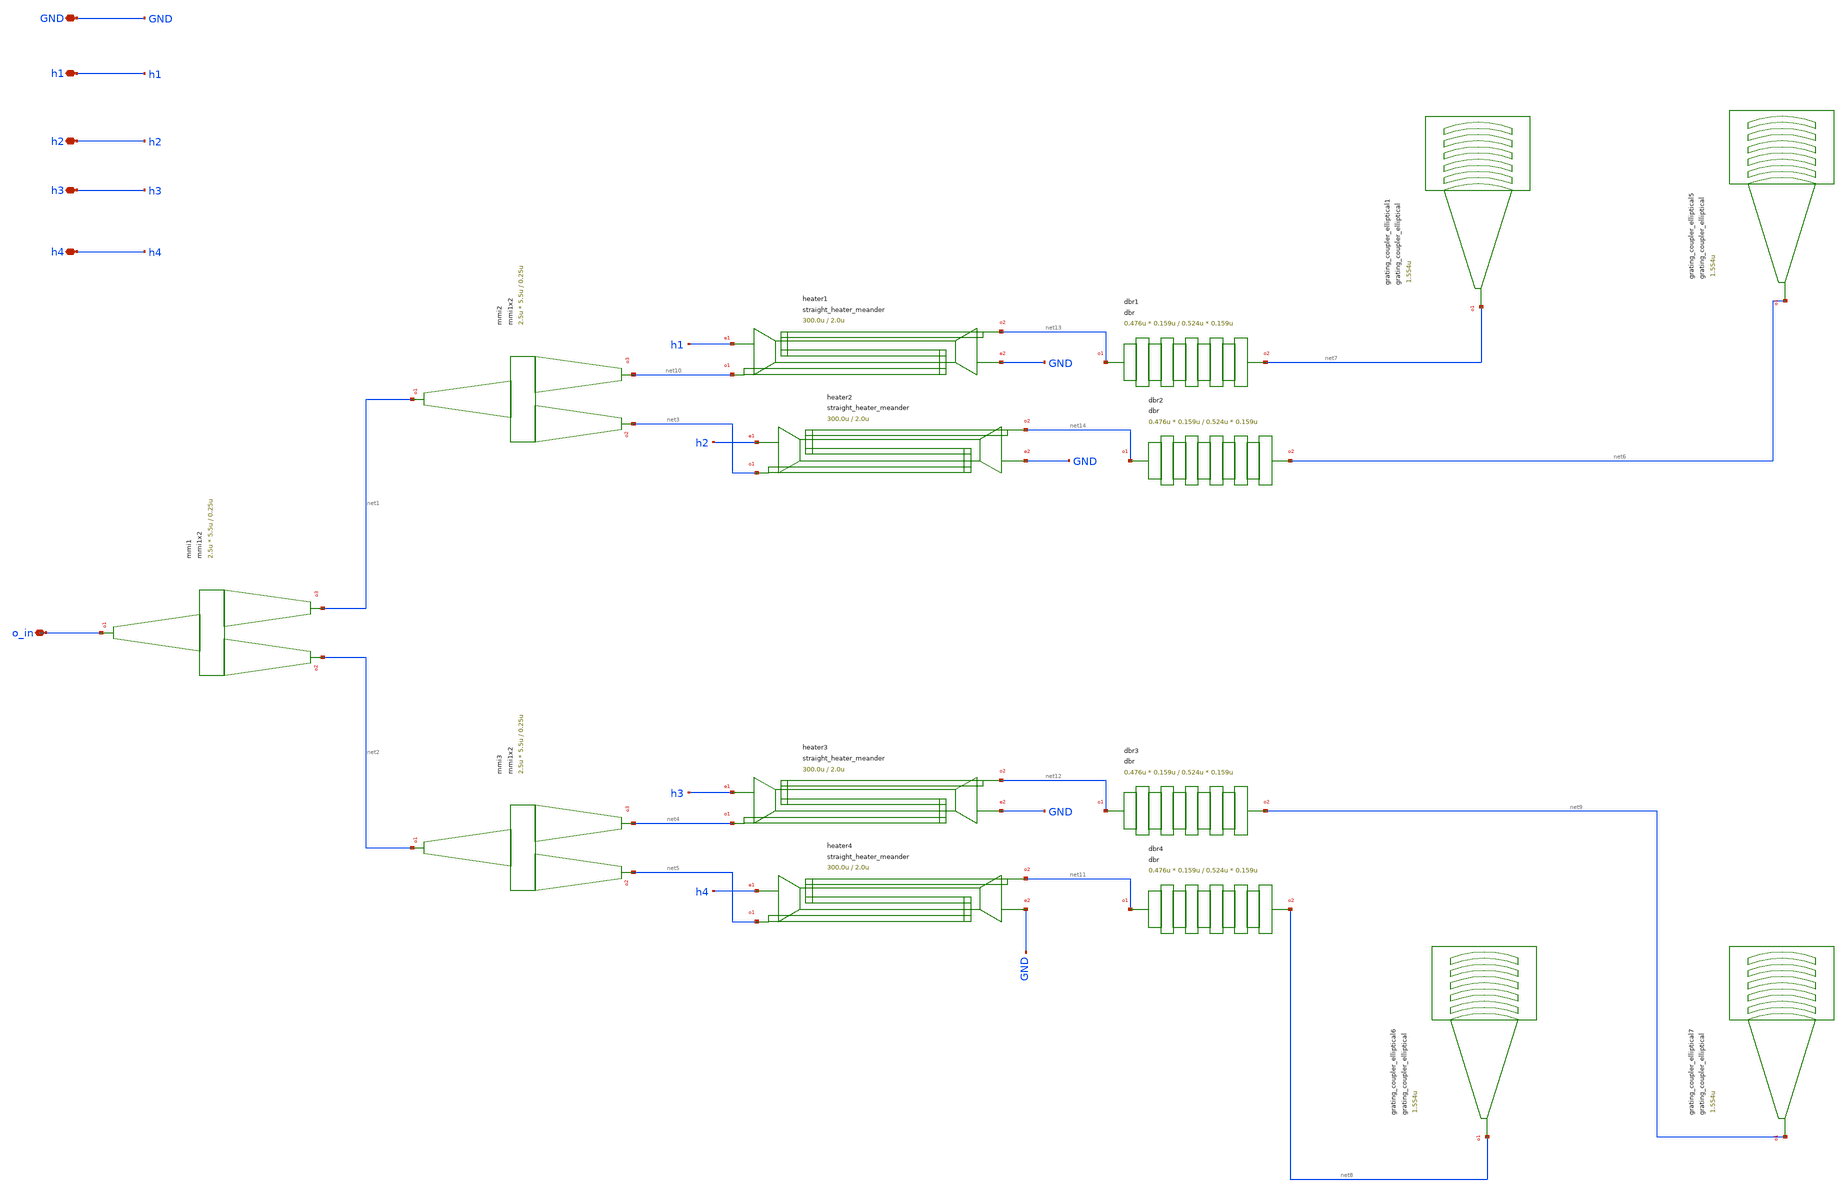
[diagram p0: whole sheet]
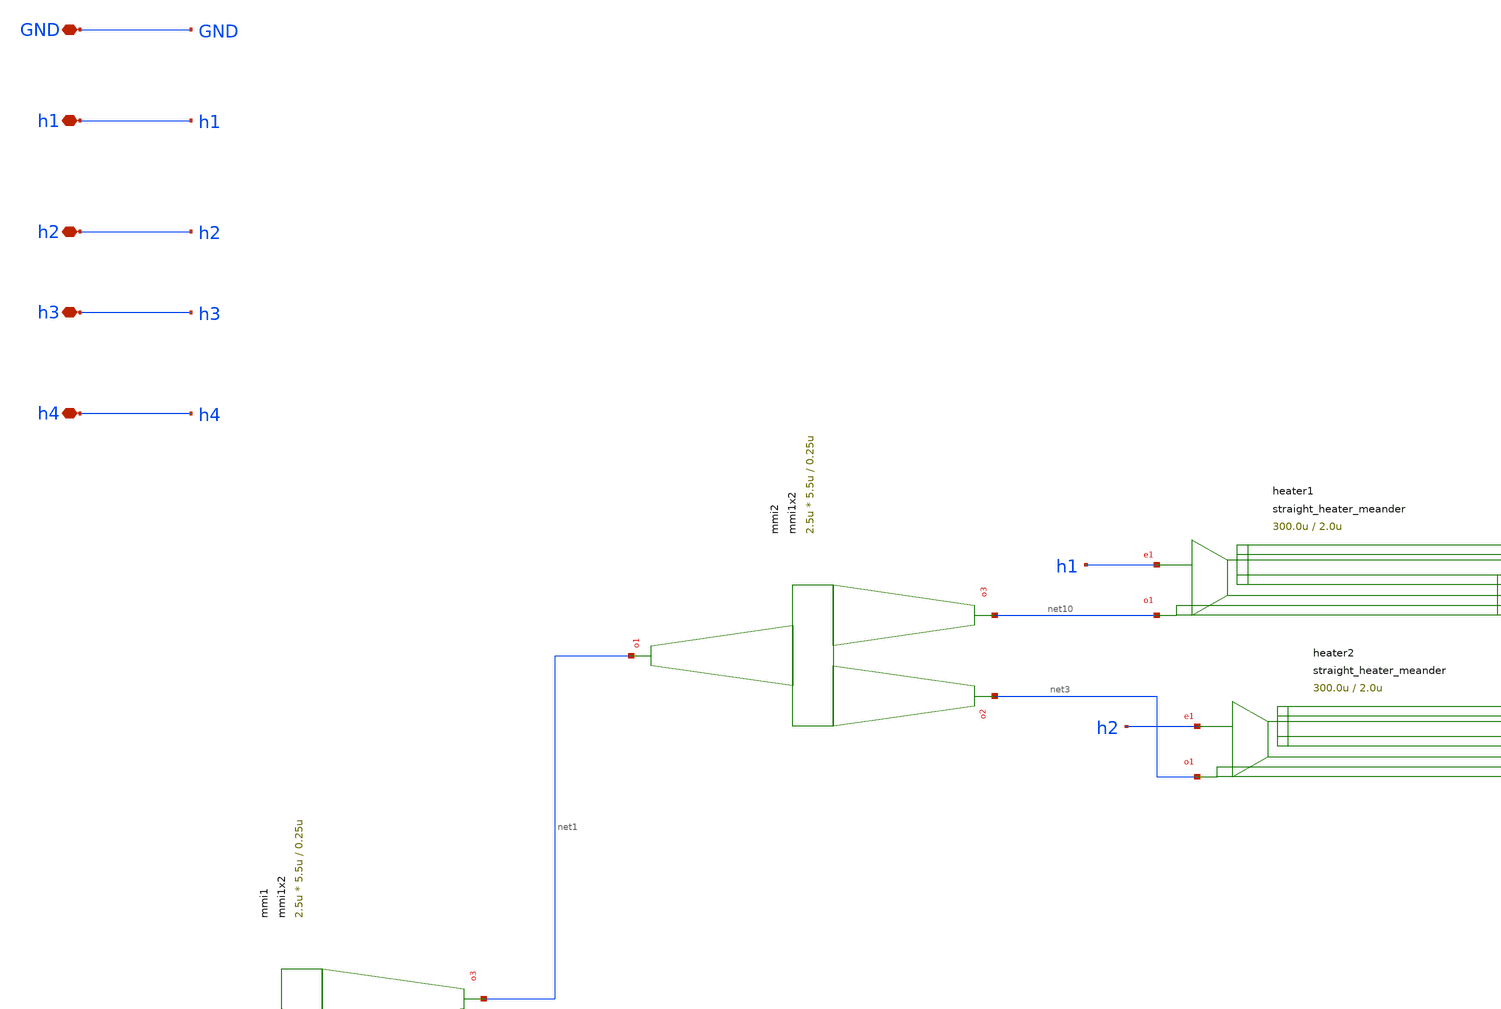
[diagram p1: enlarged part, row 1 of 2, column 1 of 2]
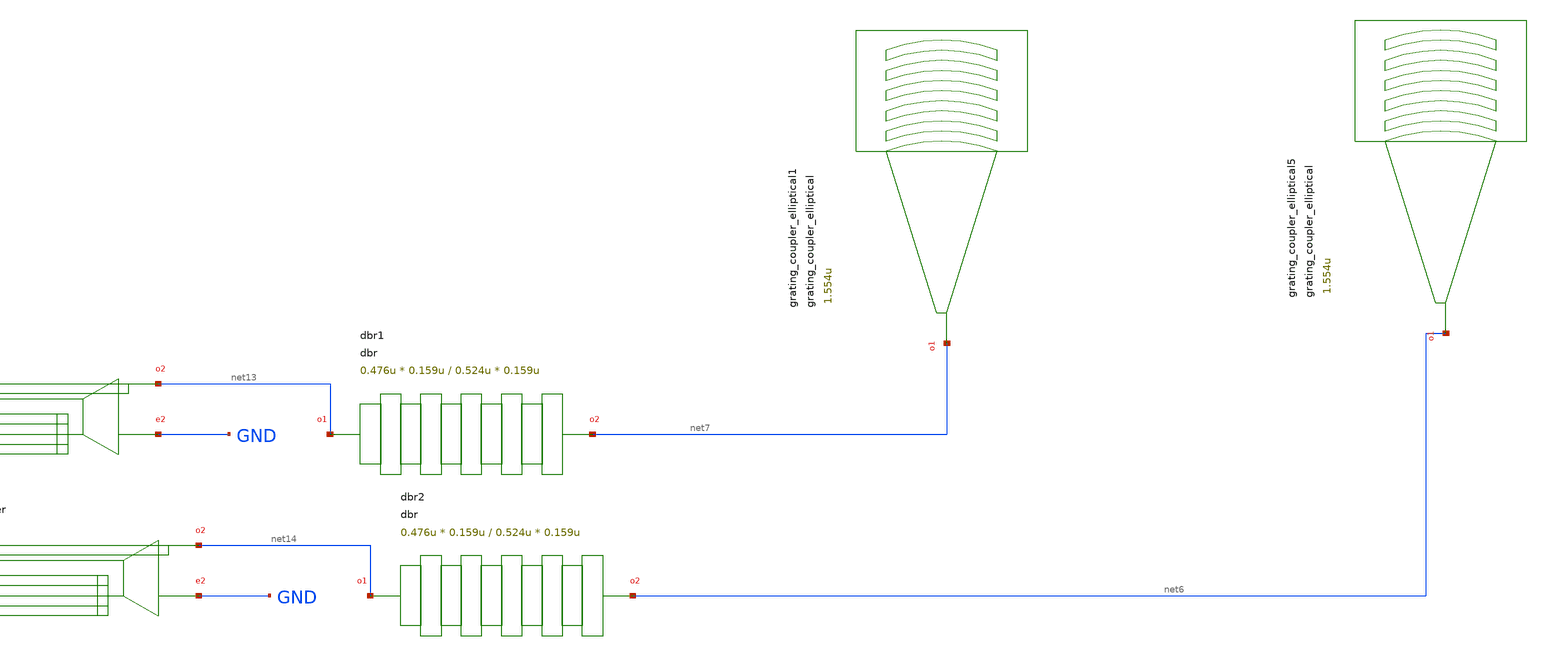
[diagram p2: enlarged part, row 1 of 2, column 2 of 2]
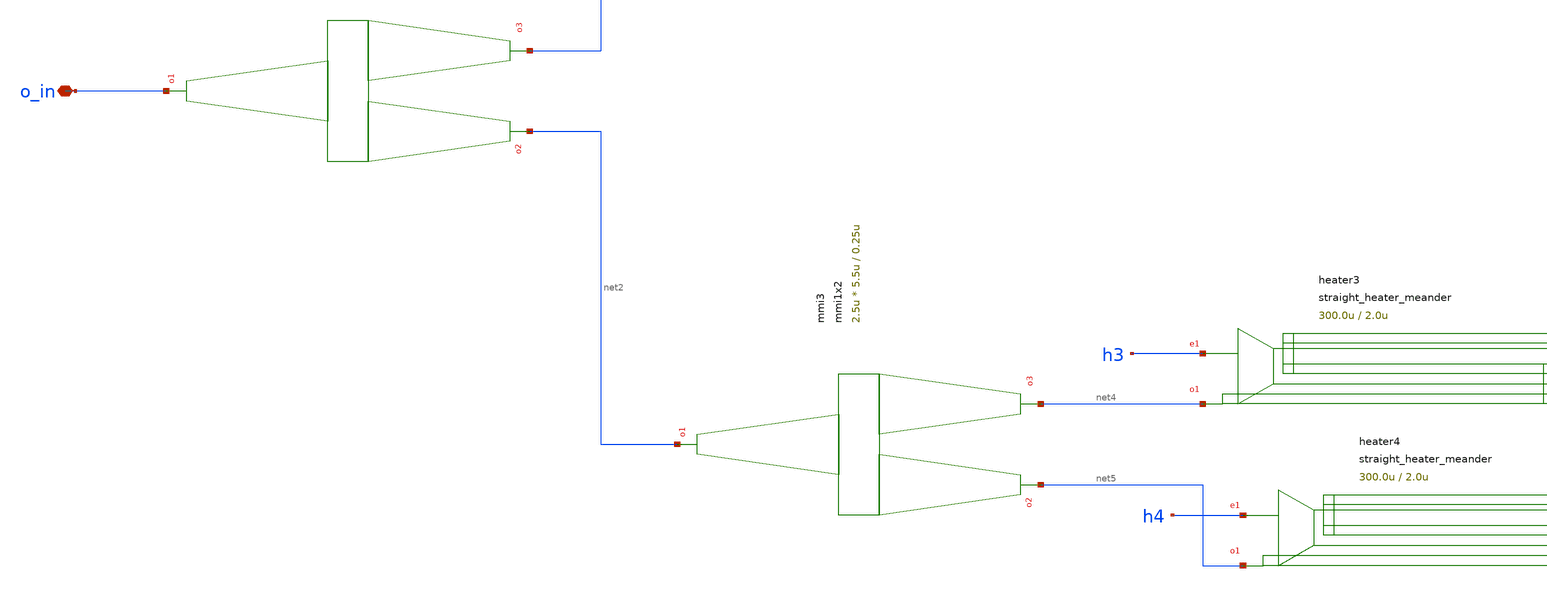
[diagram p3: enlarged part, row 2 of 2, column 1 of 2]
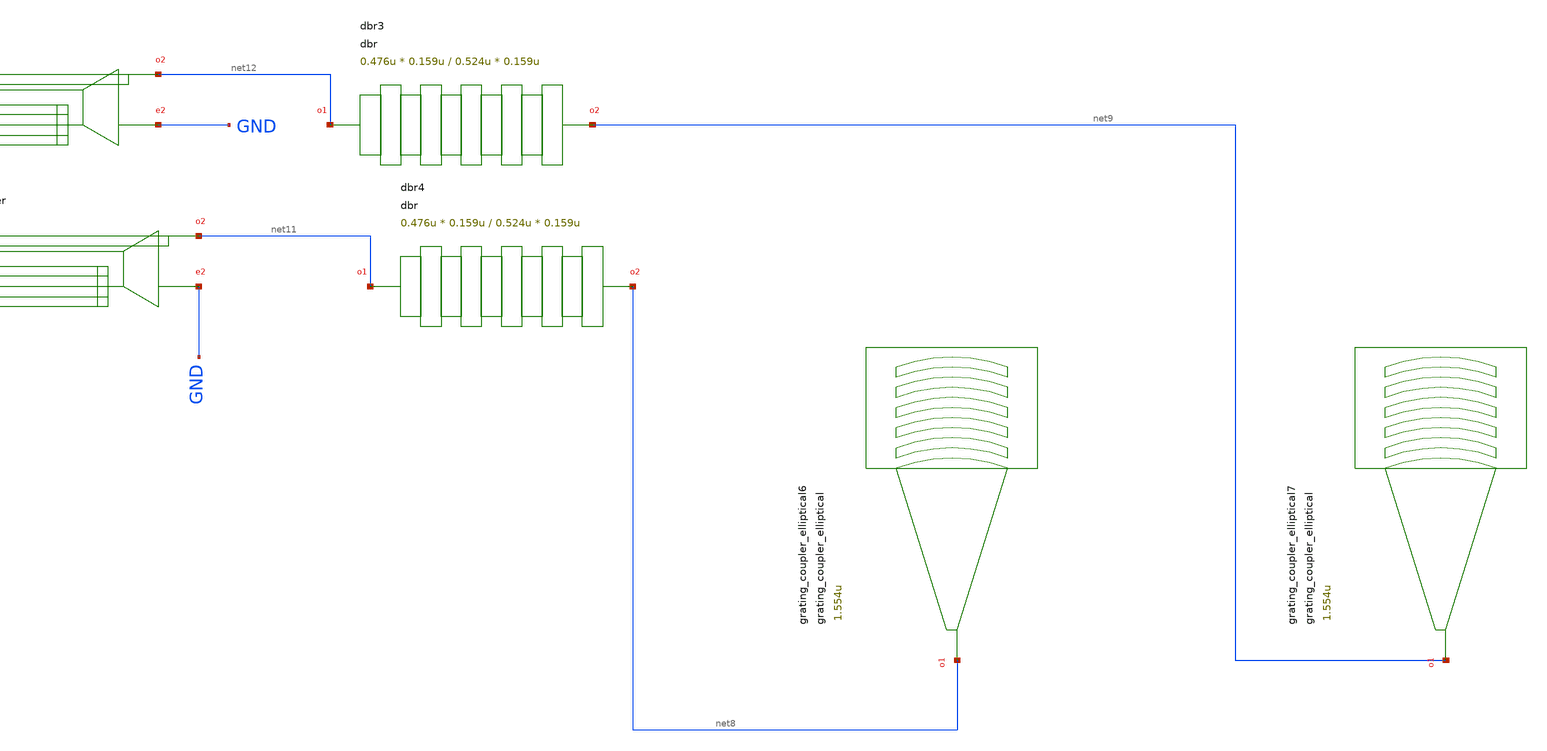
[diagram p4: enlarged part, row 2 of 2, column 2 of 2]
** sch_path: klayout/lvs/testing/testcases/unit/lidar_device/lidar.sch
**.subckt lidar o_in GND h1 h2 h3 h4
*.iopin o_in
*.iopin GND
*.iopin h1
*.iopin h2
*.iopin h3
*.iopin h4
Pmmi1 o_in net2 net1 mmi1x2 width=0.5u width_taper=1u length_taper=10u length_mmi=5.5u
+ width_mmi=2.5u gap_mmi=0.25u
Pmmi2 net1 net3 net10 mmi1x2 width=0.5u width_taper=1u length_taper=10u length_mmi=5.5u
+ width_mmi=2.5u gap_mmi=0.25u
Pmmi3 net2 net5 net4 mmi1x2 width=0.5u width_taper=1u length_taper=10u length_mmi=5.5u
+ width_mmi=2.5u gap_mmi=0.25u
Pheater1 net10 net13 h1 GND straight_heater_meander length=300.0u spacing=2.0u heater_width=2.5u
+ extension_length=15.0u radius=90u heater_taper_length=10.0u taper_length=10.0u
Pheater2 net3 net14 h2 GND straight_heater_meander length=300.0u spacing=2.0u heater_width=2.5u
+ extension_length=15.0u radius=90u heater_taper_length=10.0u taper_length=10.0u
Pheater3 net4 net12 h3 GND straight_heater_meander length=300.0u spacing=2.0u heater_width=2.5u
+ extension_length=15.0u radius=90u heater_taper_length=10.0u taper_length=10.0u
Pheater4 net5 net11 h4 GND straight_heater_meander length=300.0u spacing=2.0u heater_width=2.5u
+ extension_length=15.0u radius=90u heater_taper_length=10.0u taper_length=10.0u
Pdbr1 net13 net7 dbr w1=0.476u l1=0.159u w2=0.524u l2=0.159u n=100
Pdbr2 net14 net6 dbr w1=0.476u l1=0.159u w2=0.524u l2=0.159u n=100
Pdbr3 net12 net9 dbr w1=0.476u l1=0.159u w2=0.524u l2=0.159u n=100
Pdbr4 net11 net8 dbr w1=0.476u l1=0.159u w2=0.524u l2=0.159u n=100
Pgrating_coupler_elliptical1 net7 grating_coupler_elliptical taper_length=15u taper_angle=40.0
+ wavelength=1.554u fiber_angle=15.0 grating_line_width=0.343u n_periods=30 slab_xmin=-1.0u slab_offset=2.0u
Pgrating_coupler_elliptical5 net6 grating_coupler_elliptical taper_length=15u taper_angle=40.0
+ wavelength=1.554u fiber_angle=15.0u grating_line_width=0.343u n_periods=30 slab_xmin=-1.0u slab_offset=2.0u
Pgrating_coupler_elliptical6 net8 grating_coupler_elliptical taper_length=15u taper_angle=40.0
+ wavelength=1.554u fiber_angle=15.0u grating_line_width=0.343u n_periods=30 slab_xmin=-1.0u slab_offset=2.0u
Pgrating_coupler_elliptical7 net9 grating_coupler_elliptical taper_length=15u taper_angle=40.0u
+ wavelength=1.554u fiber_angle=15.0 grating_line_width=0.343u n_periods=30 slab_xmin=-1.0u slab_offset=2.0u
**.ends
.end
